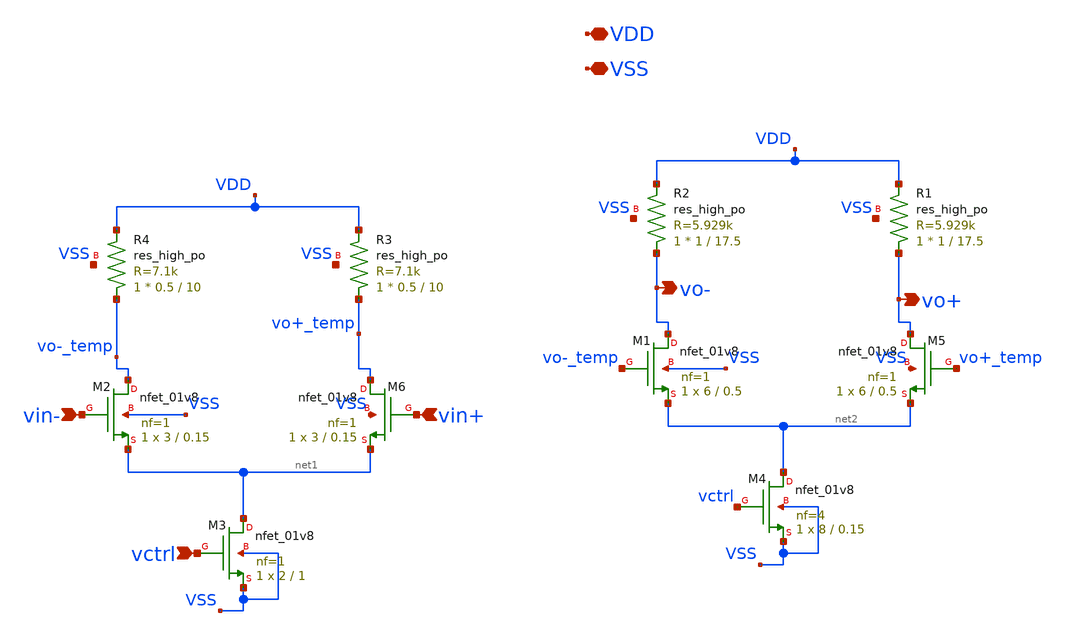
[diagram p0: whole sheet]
** sch_path: xschem/diff_amp_inv.sch
**.subckt diff_amp_inv VDD VSS vin- vctrl vin+ vo+ vo-
*.iopin VDD
*.iopin VSS
*.ipin vin-
*.ipin vctrl
*.ipin vin+
*.opin vo+
*.opin vo-
XM2 vo-_temp vin- net1 VSS sky130_fd_pr__nfet_01v8 L=0.15 W=3 nf=1 ad='int((nf+1)/2) * W/nf * 0.29' as='int((nf+2)/2) * W/nf * 0.29'
+ pd='2*int((nf+1)/2) * (W/nf + 0.29)' ps='2*int((nf+2)/2) * (W/nf + 0.29)' nrd='0.29 / W' nrs='0.29 / W'
+ sa=0 sb=0 sd=0 mult=1 m=1
XM3 net1 vctrl VSS VSS sky130_fd_pr__nfet_01v8 L=1 W=2 nf=1 ad='int((nf+1)/2) * W/nf * 0.29' as='int((nf+2)/2) * W/nf * 0.29'
+ pd='2*int((nf+1)/2) * (W/nf + 0.29)' ps='2*int((nf+2)/2) * (W/nf + 0.29)' nrd='0.29 / W' nrs='0.29 / W'
+ sa=0 sb=0 sd=0 mult=1 m=1
XM6 vo+_temp vin+ net1 VSS sky130_fd_pr__nfet_01v8 L=0.15 W=3 nf=1 ad='int((nf+1)/2) * W/nf * 0.29' as='int((nf+2)/2) * W/nf * 0.29'
+ pd='2*int((nf+1)/2) * (W/nf + 0.29)' ps='2*int((nf+2)/2) * (W/nf + 0.29)' nrd='0.29 / W' nrs='0.29 / W'
+ sa=0 sb=0 sd=0 mult=1 m=1
XR3 vo+_temp VDD VSS sky130_fd_pr__res_high_po W=0.5 L=10 mult=1 m=1
XR4 vo-_temp VDD VSS sky130_fd_pr__res_high_po W=0.5 L=10 mult=1 m=1
XM1 vo- vo-_temp net2 VSS sky130_fd_pr__nfet_01v8 L=0.5 W=6 nf=1 ad='int((nf+1)/2) * W/nf * 0.29' as='int((nf+2)/2) * W/nf * 0.29'
+ pd='2*int((nf+1)/2) * (W/nf + 0.29)' ps='2*int((nf+2)/2) * (W/nf + 0.29)' nrd='0.29 / W' nrs='0.29 / W'
+ sa=0 sb=0 sd=0 mult=1 m=1
XM4 net2 vctrl VSS VSS sky130_fd_pr__nfet_01v8 L=0.15 W=8 nf=4 ad='int((nf+1)/2) * W/nf * 0.29' as='int((nf+2)/2) * W/nf * 0.29'
+ pd='2*int((nf+1)/2) * (W/nf + 0.29)' ps='2*int((nf+2)/2) * (W/nf + 0.29)' nrd='0.29 / W' nrs='0.29 / W'
+ sa=0 sb=0 sd=0 mult=1 m=1
XM5 vo+ vo+_temp net2 VSS sky130_fd_pr__nfet_01v8 L=0.5 W=6 nf=1 ad='int((nf+1)/2) * W/nf * 0.29' as='int((nf+2)/2) * W/nf * 0.29'
+ pd='2*int((nf+1)/2) * (W/nf + 0.29)' ps='2*int((nf+2)/2) * (W/nf + 0.29)' nrd='0.29 / W' nrs='0.29 / W'
+ sa=0 sb=0 sd=0 mult=1 m=1
XR1 vo+ VDD VSS sky130_fd_pr__res_high_po W=1 L=17.5 mult=1 m=1
XR2 vo- VDD VSS sky130_fd_pr__res_high_po W=1 L=17.5 mult=1 m=1
**.ends
.end
